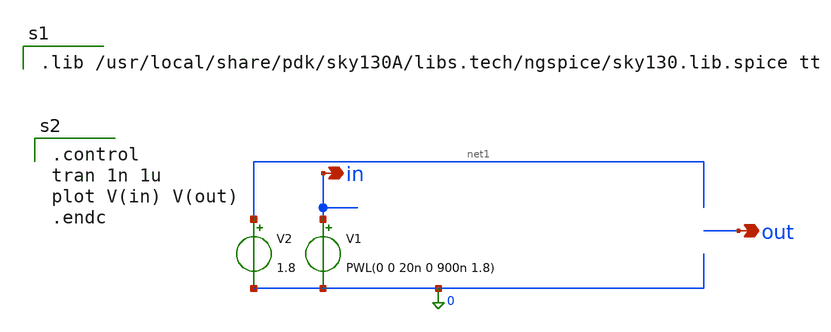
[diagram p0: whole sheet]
** sch_path: xschem/inverter_tb.sch
**.subckt inverter_tb out in
*.opin out
*.opin in
V1 in 0 PWL(0 0 20n 0 900n 1.8)
V2 net1 0 1.8
**** begin user architecture code

.lib /usr/local/share/pdk/sky130A/libs.tech/ngspice/sky130.lib.spice tt


.control
tran 1n 1u
plot V(in) V(out)
.endc

**** end user architecture code
**.ends
.end
